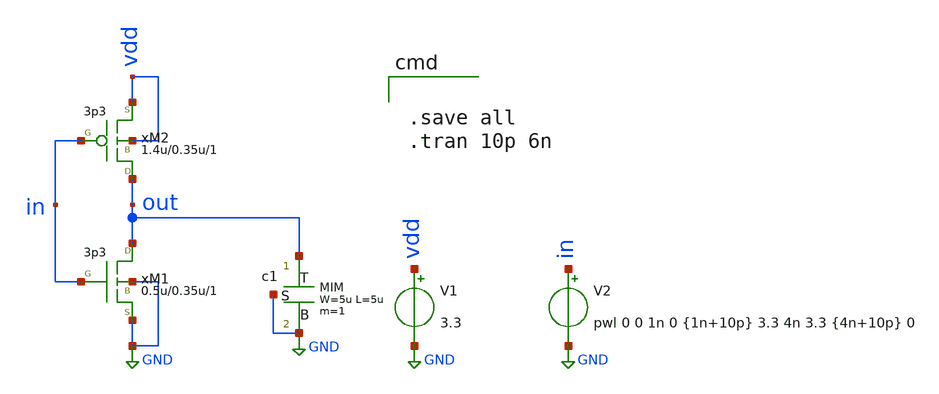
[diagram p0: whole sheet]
** sch_path: xschem/gen18_examples/inv.sch
**.subckt inv
V1 vdd GND 3.3
V2 in GND pwl 0 0 1n 0 {1n+10p} 3.3 4n 3.3 {4n+10p} 0
xc1 out GND GND cmim w=5u l=5u m=1
xM1 out in GND GND nmos33 w=0.5u l=0.35u m=1
xM2 out in vdd vdd pmos33 w=1.4u l=0.35u m=1
**** begin user architecture code

.save all
.tran 10p 6n

.include  [path_head [abs_sym_path gen18/gen18models.sym] 3]/mdl/gen18.inc
**** end user architecture code
**.ends
.GLOBAL GND
.end
